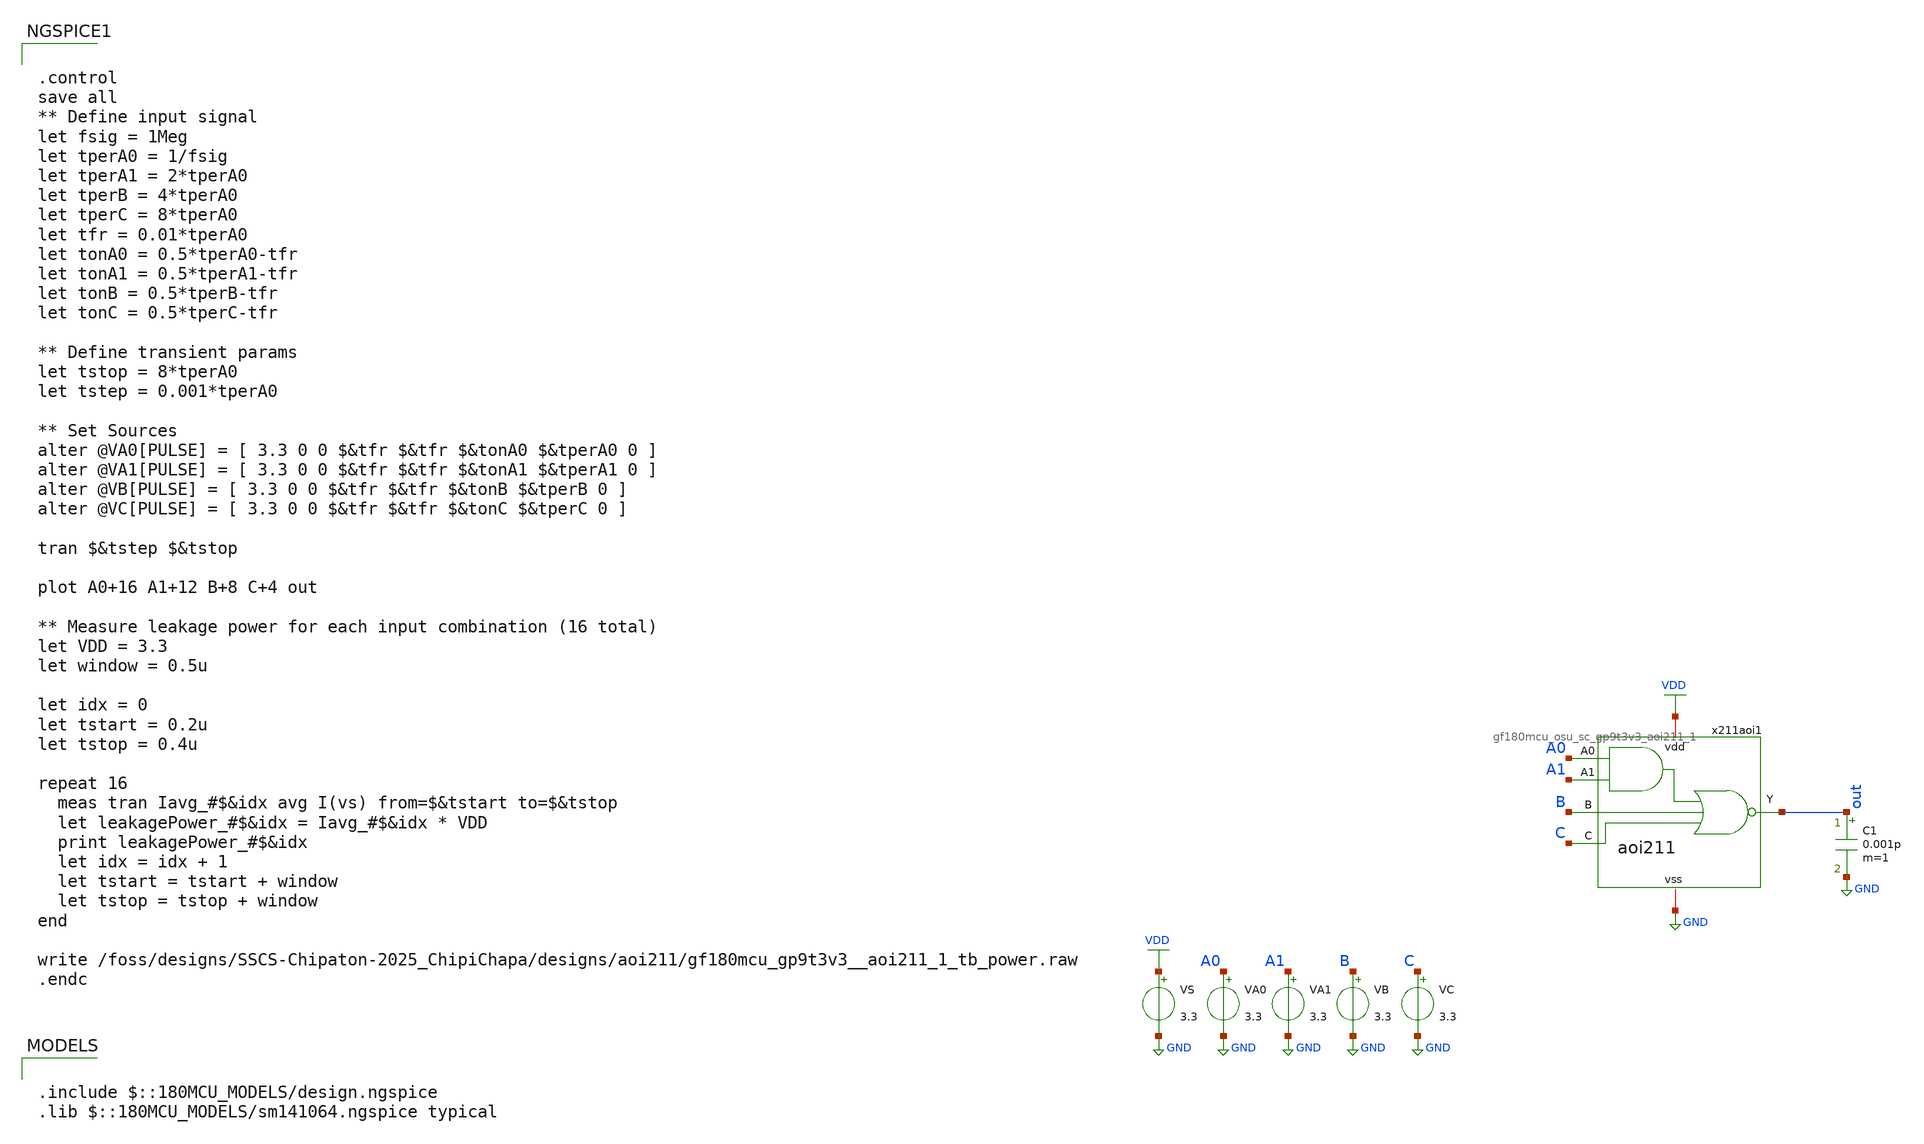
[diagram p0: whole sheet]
** sch_path: designs/aoi211/gf180mcu_osu_sc_gp9t3v3_aoi211_1_tb_power.sch
**.subckt gf180mcu_osu_sc_gp9t3v3_aoi211_1_tb_power
VA0 A0 GND 3.3
VA1 A1 GND 3.3
VB B GND 3.3
VC C GND 3.3
VS VDD GND 3.3
x211aoi1 VDD A1 A0 B C out GND gf180mcu_osu_sc_gp9t3v3_aoi211_1
C1 out GND 0.001p m=1
**** begin user architecture code


.control
save all
** Define input signal
let fsig = 1Meg
let tperA0 = 1/fsig
let tperA1 = 2*tperA0
let tperB = 4*tperA0
let tperC = 8*tperA0
let tfr = 0.01*tperA0
let tonA0 = 0.5*tperA0-tfr
let tonA1 = 0.5*tperA1-tfr
let tonB = 0.5*tperB-tfr
let tonC = 0.5*tperC-tfr

** Define transient params
let tstop = 8*tperA0
let tstep = 0.001*tperA0

** Set Sources
alter @VA0[PULSE] = [ 3.3 0 0 $&tfr $&tfr $&tonA0 $&tperA0 0 ]
alter @VA1[PULSE] = [ 3.3 0 0 $&tfr $&tfr $&tonA1 $&tperA1 0 ]
alter @VB[PULSE] = [ 3.3 0 0 $&tfr $&tfr $&tonB $&tperB 0 ]
alter @VC[PULSE] = [ 3.3 0 0 $&tfr $&tfr $&tonC $&tperC 0 ]

tran $&tstep $&tstop

plot A0+16 A1+12 B+8 C+4 out

** Measure leakage power for each input combination (16 total)
let VDD = 3.3
let window = 0.5u

let idx = 0
let tstart = 0.2u
let tstop = 0.4u

repeat 16
  meas tran Iavg_#$&idx avg I(vs) from=$&tstart to=$&tstop
  let leakagePower_#$&idx = Iavg_#$&idx * VDD
  print leakagePower_#$&idx
  let idx = idx + 1
  let tstart = tstart + window
  let tstop = tstop + window
end

write
+ /foss/designs/SSCS-Chipaton-2025_ChipiChapa/designs/aoi211/gf180mcu_gp9t3v3__aoi211_1_tb_power.raw
.endc



.include $::180MCU_MODELS/design.ngspice
.lib $::180MCU_MODELS/sm141064.ngspice typical

**** end user architecture code
**.ends
.GLOBAL GND
.GLOBAL VDD
.end
